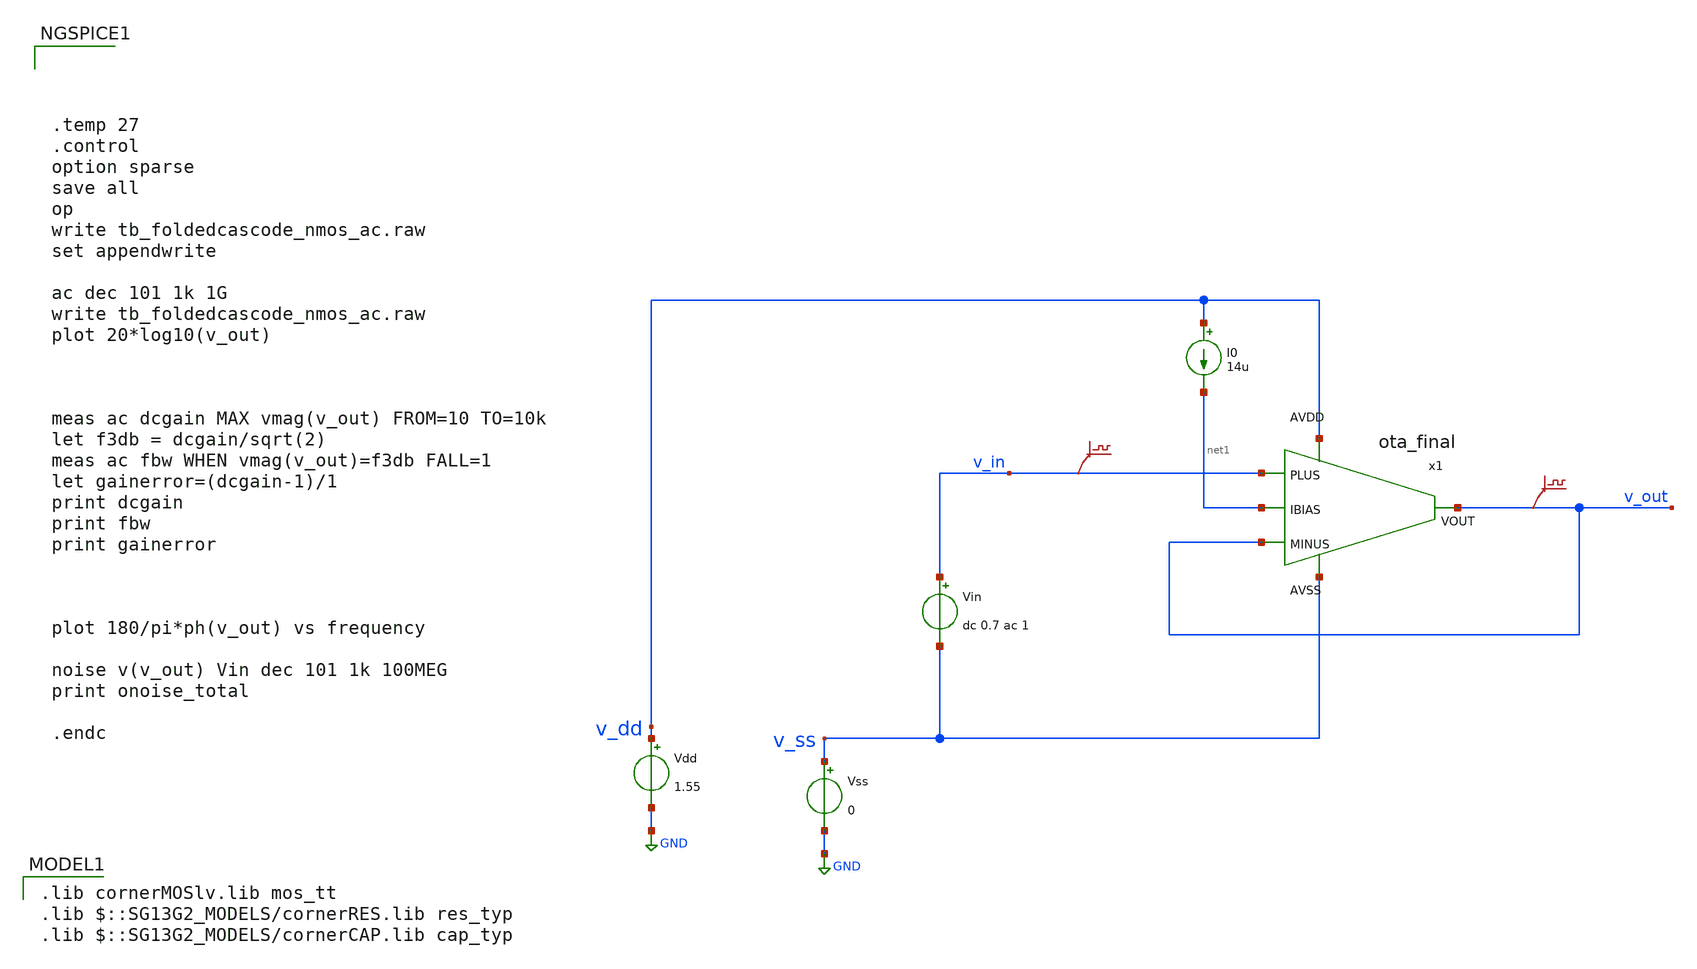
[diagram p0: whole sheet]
** sch_path: Error_amplifier_block/design_data/xschem/tb_ota_final_ac.sch
* (c) 2025 Thesis_HP, Apache-2.0 license
**.subckt tb_ota_final_ac
Vss v_ss GND 0
Vdd v_dd GND 1.55
Vin v_in v_ss dc 0.7 ac 1
.save v(v_in)
I0 v_dd net1 14u
.save v(v_out)
x1 v_dd net1 v_out v_out v_in v_ss ota_final
**** begin user architecture code




.temp 27
.control
option sparse
save all
op
write tb_foldedcascode_nmos_ac.raw
set appendwrite

ac dec 101 1k 1G
write tb_foldedcascode_nmos_ac.raw
plot 20*log10(v_out)



meas ac dcgain MAX vmag(v_out) FROM=10 TO=10k
let f3db = dcgain/sqrt(2)
meas ac fbw WHEN vmag(v_out)=f3db FALL=1
let gainerror=(dcgain-1)/1
print dcgain
print fbw
print gainerror



plot 180/pi*ph(v_out) vs frequency

noise v(v_out) Vin dec 101 1k 100MEG
print onoise_total

.endc


 .lib cornerMOSlv.lib mos_tt
.lib $::SG13G2_MODELS/cornerRES.lib res_typ
.lib $::SG13G2_MODELS/cornerCAP.lib cap_typ

**** end user architecture code
**.ends

* expanding   symbol:  ota_final.sym # of pins=6
** sym_path: Error_amplifier_block/design_data/xschem/ota_final.sym
** sch_path: Error_amplifier_block/design_data/xschem/ota_final.sch
.subckt ota_final AVDD IBIAS VOUT MINUS PLUS AVSS
*.ipin AVSS
*.ipin IBIAS
*.ipin AVDD
*.ipin PLUS
*.ipin MINUS
*.opin VOUT
XM23 IBIAS IBIAS AVSS AVSS sg13_lv_nmos w=8.5u l=5u ng=4 m=1 mm_ok=1
XM24 net7 IBIAS AVSS AVSS sg13_lv_nmos w=8.5u l=5u ng=4 m=1 mm_ok=1
XM11 net7 net2 net1 AVDD sg13_lv_pmos w=14u l=2u ng=4 m=1 mm_ok=1
XM12 net1 net1 AVDD AVDD sg13_lv_pmos w=14u l=2u ng=4 m=1 mm_ok=1
XM18 AVSS net2 net5 AVDD sg13_lv_pmos w=14u l=0.5u ng=4 m=1 mm_ok=1
XM17 net5 net1 AVDD AVDD sg13_lv_pmos w=14u l=2u ng=4 m=1 mm_ok=1
XM9 net4 net1 AVDD AVDD sg13_lv_pmos w=14u l=2u ng=4 m=1 mm_ok=1
XM5 net2 net5 net4 AVDD sg13_lv_pmos w=14u l=2u ng=4 m=1 mm_ok=1
XM7 net2 net12 net3 AVSS sg13_lv_nmos w=3u l=2u ng=2 m=1 mm_ok=1
XM3 net3 net2 AVSS AVSS sg13_lv_nmos w=3u l=2u ng=2 m=1 mm_ok=1
XM30 net6 IBIAS AVSS AVSS sg13_lv_nmos w=8.5u l=5u ng=4 m=1 mm_ok=1
XM1 net4 PLUS net6 AVSS sg13_lv_nmos w=6u l=1u ng=2 m=1 mm_ok=1
XM2 net8 MINUS net6 AVSS sg13_lv_nmos w=6u l=1u ng=2 m=1 mm_ok=1
XM37 net8 AVSS AVSS AVSS sg13_lv_nmos w=6u l=1u ng=2 m=1 mm_ok=1
XM6 VOUT net5 net8 AVDD sg13_lv_pmos w=14u l=2u ng=4 m=1 mm_ok=1
XM0 net8 net1 AVDD AVDD sg13_lv_pmos w=14u l=2u ng=4 m=1 mm_ok=1
XM8 VOUT net12 net9 AVSS sg13_lv_nmos w=3u l=2u ng=2 m=1 mm_ok=1
XM4 net9 net2 AVSS AVSS sg13_lv_nmos w=3u l=2u ng=2 m=1 mm_ok=1
XM29 net9 AVSS AVSS AVSS sg13_lv_nmos w=3u l=2u ng=2 m=1 mm_ok=1
XM28 VOUT AVSS AVSS AVSS sg13_lv_nmos w=3u l=2u ng=2 m=1 mm_ok=1
XM32 net8 AVDD AVDD AVDD sg13_lv_pmos w=14u l=2u ng=4 m=1 mm_ok=1
XM33 VOUT AVDD AVDD AVDD sg13_lv_pmos w=7u l=2u ng=2 m=1 mm_ok=1
XM13 net10 net1 AVDD AVDD sg13_lv_pmos w=14u l=2u ng=4 m=1 mm_ok=1
XM15 net10 VOUT net11 AVSS sg13_lv_nmos w=3u l=2u ng=2 m=1 mm_ok=1
XM16 net11 net11 AVSS AVSS sg13_lv_nmos w=3u l=2u ng=2 m=1 mm_ok=1
XM14 net12 net11 AVSS AVSS sg13_lv_nmos w=3u l=2u ng=2 m=1 mm_ok=1
XM10 AVDD VOUT net12 AVSS sg13_lv_nmos w=15u l=0.5u ng=4 m=1 mm_ok=1
XM36 net4 AVSS AVSS AVSS sg13_lv_nmos w=6u l=1u ng=2 m=1 mm_ok=1
XM34 net2 AVDD AVDD AVDD sg13_lv_pmos w=7u l=2u ng=2 m=1 mm_ok=1
XM27 net3 AVSS AVSS AVSS sg13_lv_nmos w=3u l=2u ng=2 m=1 mm_ok=1
XM26 net2 AVSS AVSS AVSS sg13_lv_nmos w=3u l=2u ng=2 m=1 mm_ok=1
XM35 net1 AVDD AVDD AVDD sg13_lv_pmos w=7u l=2u ng=2 m=1 mm_ok=1
XM31 net11 AVSS AVSS AVSS sg13_lv_nmos w=3u l=2u ng=2 m=1 mm_ok=1
XC2 VOUT AVSS cap_cmim w=25.82e-6 l=25.82e-6 m=1 mm_ok=1
.ends

.GLOBAL GND
.end
